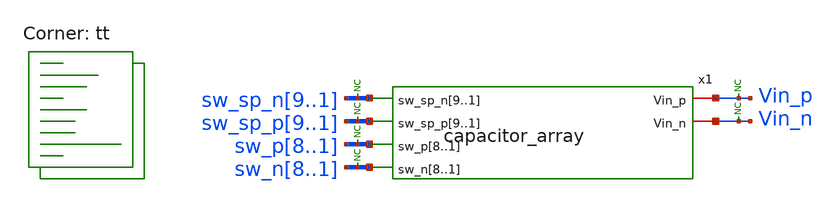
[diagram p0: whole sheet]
** sch_path: xschem/tests/capacitor_array/capacitor_array_test.sch
**.subckt capacitor_array_test
x1 Vin_p sw_sp_n9 sw_sp_n8 sw_sp_n7 sw_sp_n6 sw_sp_n5 sw_sp_n4 sw_sp_n3 sw_sp_n2 sw_sp_n1 sw_sp_p9
+ sw_sp_p8 sw_sp_p7 sw_sp_p6 sw_sp_p5 sw_sp_p4 sw_sp_p3 sw_sp_p2 sw_sp_p1 Vin_n sw_p8 sw_p7 sw_p6 sw_p5 sw_p4
+ sw_p3 sw_p2 sw_p1 sw_n8 sw_n7 sw_n6 sw_n5 sw_n4 sw_n3 sw_n2 sw_n1 capacitor_array unit_cap_w=25
+ unit_cap_l=25
* noconn sw_sp_n[9..1]
* noconn sw_sp_p[9..1]
* noconn sw_p[8..1]
* noconn sw_n[8..1]
* noconn Vin_p
* noconn Vin_n
**** begin user architecture code
 *.lib $::SKYWATER_MODELS/sky130.lib.spice tt
.include $::SKYWATER_STDCELLS/sky130_fd_sc_hd.spice


.options acct list
.temp 25
*vvcc VDD 0 dc 1.8
*vvss VSS 0 0

v_sp_n1 sw_sp_n1 gnd  PULSE(0 1.8V 0 1ns 1ns 5us 200us)
v_sp_n2 sw_sp_n2 gnd  PULSE(0 1.8V 0 1ns 1ns 10us 200us)
v_sp_n3 sw_sp_n3 gnd  PULSE(0 1.8V 0 1ns 1ns 15us 200us)
v_sp_n4 sw_sp_n4 gnd  PULSE(0 1.8V 0 1ns 1ns 20us 200us)
v_sp_n5 sw_sp_n5 gnd  PULSE(0 1.8V 0 1ns 1ns 25us 200us)
v_sp_n6 sw_sp_n6 gnd  PULSE(0 1.8V 0 1ns 1ns 30us 200us)
v_sp_n7 sw_sp_n7 gnd  PULSE(0 1.8V 0 1ns 1ns 35us 200us)
v_sp_n8 sw_sp_n8 gnd  PULSE(0 1.8V 0 1ns 1ns 45us 200us)
v_sp_n9 sw_sp_n9 gnd  PULSE(0 1.8V 0 1ns 1ns 50us 200us)

v_n1 sw_n1 gnd  PULSE(0 1.8V 0 1ns 1ns 55us 200us)
v_n2 sw_n2 gnd  PULSE(0 1.8V 0 1ns 1ns 60us 200us)
v_n3 sw_n3 gnd  PULSE(0 1.8V 0 1ns 1ns 65us 200us)
v_n4 sw_n4 gnd  PULSE(0 1.8V 0 1ns 1ns 70us 200us)
v_n5 sw_n5 gnd  PULSE(0 1.8V 0 1ns 1ns 75us 200us)
v_n6 sw_n6 gnd  PULSE(0 1.8V 0 1ns 1ns 80us 200us)
v_n7 sw_n7 gnd  PULSE(0 1.8V 0 1ns 1ns 85us 200us)
v_n8 sw_n8 gnd  PULSE(0 1.8V 0 1ns 1ns 90us 200us)

v_sp_p1 sw_sp_p1 gnd  PULSE(0 1.8V 0 1ns 1ns 5us 200us)
v_sp_p2 sw_sp_p2 gnd  PULSE(0 1.8V 0 1ns 1ns 10us 200us)
v_sp_p3 sw_sp_p3 gnd  PULSE(0 1.8V 0 1ns 1ns 15us 200us)
v_sp_p4 sw_sp_p4 gnd  PULSE(0 1.8V 0 1ns 1ns 20us 200us)
v_sp_p5 sw_sp_p5 gnd  PULSE(0 1.8V 0 1ns 1ns 25us 200us)
v_sp_p6 sw_sp_p6 gnd  PULSE(0 1.8V 0 1ns 1ns 30us 200us)
v_sp_p7 sw_sp_p7 gnd  PULSE(0 1.8V 0 1ns 1ns 35us 200us)
v_sp_p8 sw_sp_p8 gnd  PULSE(0 1.8V 0 1ns 1ns 45us 200us)
v_sp_p9 sw_sp_p9 gnd  PULSE(0 1.8V 0 1ns 1ns 50us 200us)

v_p1 sw_p1 gnd  PULSE(0 1.8V 0 1ns 1ns 55us 200us)
v_p2 sw_p2 gnd  PULSE(0 1.8V 0 1ns 1ns 60us 200us)
v_p3 sw_p3 gnd  PULSE(0 1.8V 0 1ns 1ns 65us 200us)
v_p4 sw_p4 gnd  PULSE(0 1.8V 0 1ns 1ns 70us 200us)
v_p5 sw_p5 gnd  PULSE(0 1.8V 0 1ns 1ns 75us 200us)
v_p6 sw_p6 gnd  PULSE(0 1.8V 0 1ns 1ns 80us 200us)
v_p7 sw_p7 gnd  PULSE(0 1.8V 0 1ns 1ns 85us 200us)
v_p8 sw_p8 gnd  PULSE(0 1.8V 0 1ns 1ns 90us 200us)

.control
ic v(vin_p)=1.8V
ic v(vin_n)=1.8V
save all
tran 0.1u 110u
write capacitor_array_test.raw
plot Vin_n Vin_p+2
.endc


.lib $::SKYWATER_MODELS/sky130.lib.spice tt
**** end user architecture code
**.ends
.end
